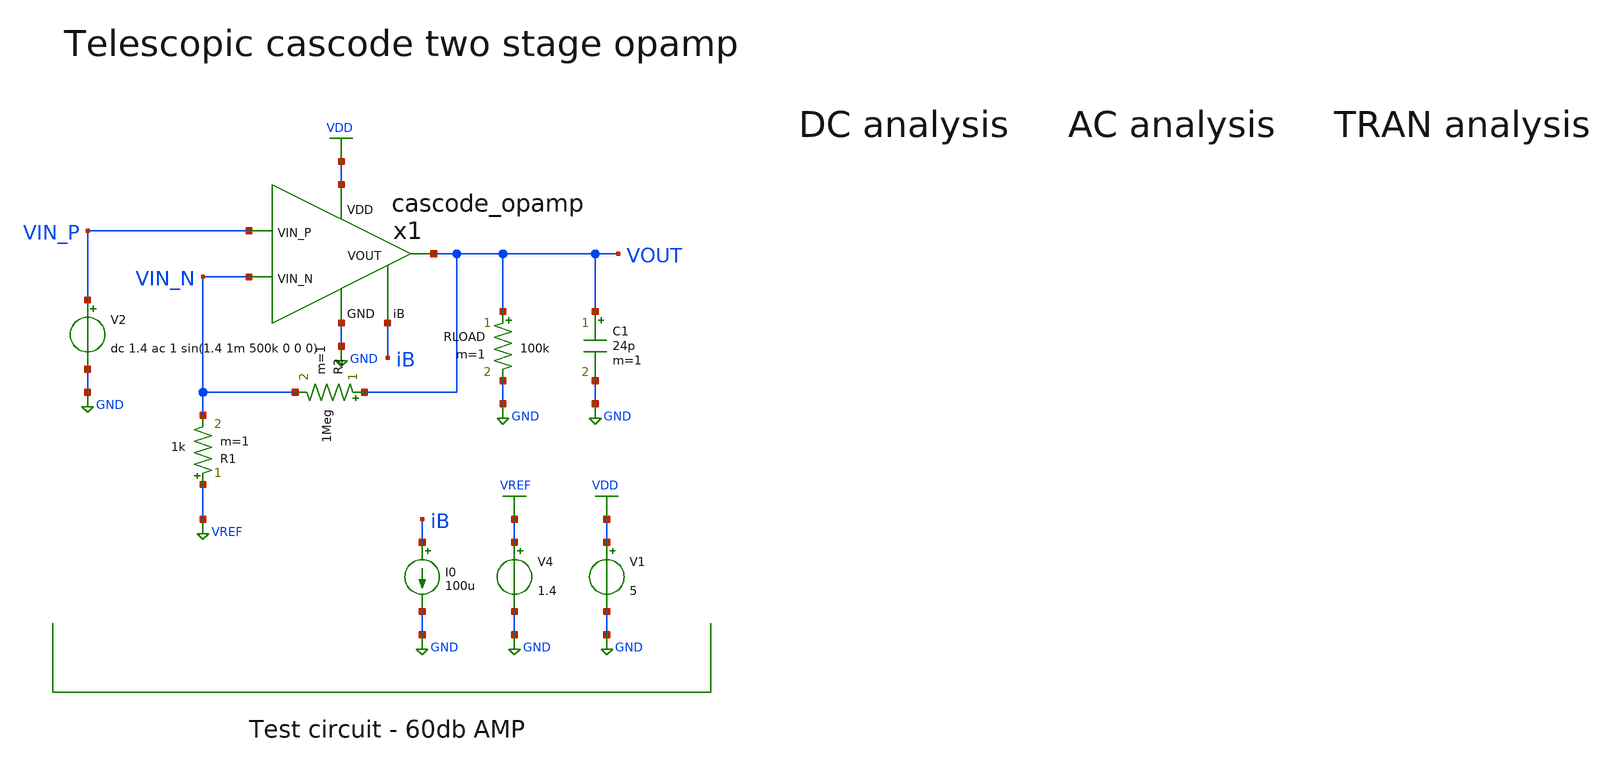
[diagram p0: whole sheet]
** sch_path: member_project/AM_Radio/Yamada3/xschem/tb_cascode_opamp.sch
**.subckt tb_cascode_opamp
V1 VDD GND 5
R2 VOUT VIN_N 1Meg m=1
V2 VIN_P GND dc 1.4 ac 1 sin(1.4 1m 500k 0 0 0)
V4 VREF GND 1.4
RLOAD VOUT GND 100k m=1
C1 VOUT GND 24p m=1
R1 VREF VIN_N 1k m=1
x1 VDD GND VIN_P VIN_N VOUT iB cascode_opamp
I0 iB GND 100u
**** begin user architecture code
 .include $::LIB/ip62_models

.control
save all
save currents
* DC analysis
dc v2 0 5 1m rload 10k 100k 20k
let dc_gain=deriv(VOUT)
write tb_cascode_opamp_dc.raw
* AC analysis
ac dec 10 1k 10Meg
let ac_gain = VOUT / vin_p
let ac_gain_db = db(ac_gain)
let ac_phase_deg = (180 / PI) * cph(ac_gain)
write tb_cascode_opamp_ac.raw
* TRAN analysis
tran 0.1u 20u
write tb_cascode_opamp_tran.raw
.endc


**** end user architecture code
**.ends

* expanding   symbol:  cascode_opamp.sym # of pins=6
** sym_path: member_project/AM_Radio/Yamada3/xschem/cascode_opamp.sym
** sch_path: member_project/AM_Radio/Yamada3/xschem/cascode_opamp.sch
.subckt cascode_opamp VDD GND VIN_P VIN_N VOUT iB
*.opin VOUT
*.ipin VIN_N
*.ipin VIN_P
*.ipin GND
*.ipin VDD
*.ipin iB
MM2 net2 net1 VDD VDD PMOS w=30u l=1u as=0 ad=0 ps=0 pd=0 nrd=0 nrs=0 m=1
MM4 OUT1 VB2 net5 GND NMOS w=10u l=1u as=0 ad=0 ps=0 pd=0 nrd=0 nrs=0 m=1
MM7 VOUT iB VDD VDD PMOS w=300u l=1u as=0 ad=0 ps=0 pd=0 nrd=0 nrs=0 m=1
MM8 VOUT OUT1 GND GND NMOS w=200u l=1u as=0 ad=0 ps=0 pd=0 nrd=0 nrs=0 m=1
MM16 net1 net1 VDD VDD PMOS w=30u l=1u as=0 ad=0 ps=0 pd=0 nrd=0 nrs=0 m=1
MM17 OUT1 net3 net2 VDD PMOS w=30u l=1u as=0 ad=0 ps=0 pd=0 nrd=0 nrs=0 m=1
MM18 net3 net3 net1 VDD PMOS w=30u l=1u as=0 ad=0 ps=0 pd=0 nrd=0 nrs=0 m=1
MM19 net3 VB2 net4 GND NMOS w=10u l=1u as=0 ad=0 ps=0 pd=0 nrd=0 nrs=0 m=1
MM20 net5 VIN_P net6 GND NMOS w=80u l=1u as=0 ad=0 ps=0 pd=0 nrd=0 nrs=0 m=1
MM21 net4 VIN_N net6 GND NMOS w=80u l=1u as=0 ad=0 ps=0 pd=0 nrd=0 nrs=0 m=1
MM22 net6 VB1 GND GND NMOS w=10u l=1u as=0 ad=0 ps=0 pd=0 nrd=0 nrs=0 m=1
MM3 net7 net11 OUT1 GND NMOS w=20u l=1u as=0 ad=0 ps=0 pd=0 nrd=0 nrs=0 m=1
CC2 net7 VOUT GND F_CSIO c=0.1p x=120u y=120u m=1
MM5 net11 net11 net8 GND NMOS w=20u l=1u as=0 ad=0 ps=0 pd=0 nrd=0 nrs=0 m=1
MM6 net8 net8 GND GND NMOS w=20u l=1u as=0 ad=0 ps=0 pd=0 nrd=0 nrs=0 m=1
MM13 VB2 VB2 VB1 GND NMOS w=10u l=1u as=0 ad=0 ps=0 pd=0 nrd=0 nrs=0 m=1
MM14 VB1 VB1 GND GND NMOS w=10u l=1u as=0 ad=0 ps=0 pd=0 nrd=0 nrs=0 m=1
MM23 VB4 VB4 VDD VDD PMOS w=30u l=1u as=0 ad=0 ps=0 pd=0 nrd=0 nrs=0 m=1
MM24 VB2 iB net9 VDD PMOS w=30u l=1u as=0 ad=0 ps=0 pd=0 nrd=0 nrs=0 m=1
MM25 net9 VB4 VDD VDD PMOS w=30u l=1u as=0 ad=0 ps=0 pd=0 nrd=0 nrs=0 m=1
MM26 iB iB VB4 VDD PMOS w=30u l=1u as=0 ad=0 ps=0 pd=0 nrd=0 nrs=0 m=1
MM1 net11 iB net10 VDD PMOS w=30u l=1u as=0 ad=0 ps=0 pd=0 nrd=0 nrs=0 m=1
MM9 net10 VB4 VDD VDD PMOS w=30u l=1u as=0 ad=0 ps=0 pd=0 nrd=0 nrs=0 m=1
.ends

.GLOBAL VDD
.GLOBAL GND
.GLOBAL VREF
.end
